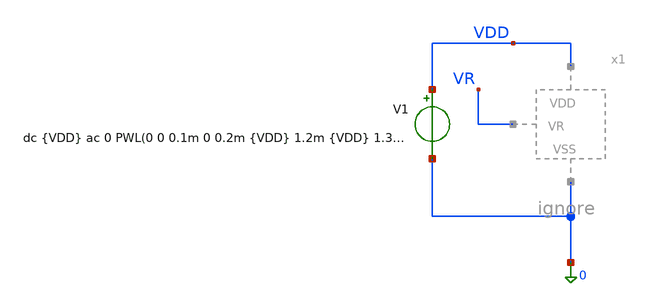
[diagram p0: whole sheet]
** sch_path: xschem/Self_Bias/self_bias_tb_pex_mc.sch
**.subckt self_bias_tb_pex_mc
V1 VDD 0 dc {VDD} ac 0 PWL(0 0 0.1m 0 0.2m {VDD} 1.2m {VDD} 1.3m 0 2m 0 3m {VDD} 4m {VDD} 4.1m 0 5m 0
+ 105m {VDD} 110m {VDD} 110.1m 0)
**** begin user architecture code


* ==============================================================================
* ENCABEZADO DEL ARCHIVO:
* Script de simulación Monte Carlo Post-Layout (PEX) para el circuito Self-Bias.
* Evalúa las 3 rampas de arranque (Trise = 100us, 1ms y 100ms) con tiempos de
* espera recortados (110.1ms totales en lugar de 410ms).
* ==============================================================================

* 1. Librería de modelos Sky130 con Mismatch (tt_mm) y netlist PEX
.lib /foss/pdks/sky130A/libs.tech/ngspice/sky130.lib.spice tt_mm
.include /foss/designs/LDO-sky130/xschem/Self_Bias/self_bias_pex.spice
x1 VDD VR 0 self_bias

.option temp=27
.option num_threads=8
.option gmin=1e-12 reltol=1e-3 abstol=1e-12 vntol=1e-6

* 2. Parámetros globales y condiciones iniciales para el PEX
.param VDD = 1.8
.param rsh_var = agauss(0, 0.005, 1)

.nodeset V(VR)=0.6
.nodeset V(x1.vgp_self)=1.0
.nodeset V(x1.vdi)=0.6
.nodeset V(x1.vdinv)=0.0

.control
let mc_runs = 100
let run = 1

set appendwrite
set filetype=ascii

echo === INICIO MONTE CARLO SELF BIAS PEX === > self_bias_mc.txt

while run <= mc_runs

    echo ======================================
    echo CORRIENDO MONTE CARLO PEX ITERACION: $&run
    echo ======================================
    echo --- ITERACION: $&run --- >> self_bias_mc.txt

    * 1. Resetear variables aleatorias y guardar VDD, VR y los 6 dedos de Mp4
    reset
    save v(VDD) v(vr) @m.x1.x2.msky130_fd_pr__pfet_01v8_lvt[id]
+ @m.x1.x7.msky130_fd_pr__pfet_01v8_lvt[id] @m.x1.x11.msky130_fd_pr__pfet_01v8_lvt[id] @m.x1.x14.msky130_fd_pr__pfet_01v8_lvt[id]
+ @m.x1.x16.msky130_fd_pr__pfet_01v8_lvt[id] @m.x1.x19.msky130_fd_pr__pfet_01v8_lvt[id]

    * 2. Análisis Transitorio corto (110.1ms totales para las 3 rampas)
    tran 1m 110.1m

    * Corriente total IBIAS (suma de los 6 dedos de Mp4 en el PEX)
    let ibias_tot = @m.x1.x2.msky130_fd_pr__pfet_01v8_lvt[id] +
+ @m.x1.x7.msky130_fd_pr__pfet_01v8_lvt[id] + @m.x1.x11.msky130_fd_pr__pfet_01v8_lvt[id] + @m.x1.x14.msky130_fd_pr__pfet_01v8_lvt[id] +
+ @m.x1.x16.msky130_fd_pr__pfet_01v8_lvt[id] + @m.x1.x19.msky130_fd_pr__pfet_01v8_lvt[id]

    write self_bias_mc_tran.raw v(VDD) v(vr) ibias_tot

    * 3. Mediciones en las 3 rampas
    * --- PULSO 1 (Trise = 100us: sube de 0.1m a 0.2m, medimos en 1ms) ---
    meas tran vr_100us FIND v(vr) AT=1m
    meas tran id_100us FIND ibias_tot AT=1m

    * --- PULSO 2 (Trise = 1ms: sube de 2m a 3m, medimos en 3.8ms) ---
    meas tran vr_1ms FIND v(vr) AT=3.8m
    meas tran id_1ms FIND ibias_tot AT=3.8m

    * --- PULSO 3 (Trise = 100ms: sube de 5m a 105m, medimos en 108ms) ---
    meas tran vr_100ms FIND v(vr) AT=108m
    meas tran id_100ms FIND ibias_tot AT=108m

    * Convertir corrientes a microamperios (uA)
    let id_uA_100us = id_100us * 1000000
    let id_uA_1ms   = id_1ms * 1000000
    let id_uA_100ms = id_100ms * 1000000

    * 4. Guardar resultados en el archivo de texto
    echo 'Resultados Iteración $&run:' >> self_bias_mc.txt
    echo '  [100us] VR = $&vr_100us V   | IBIAS = $&id_uA_100us uA' >> self_bias_mc.txt
    echo '  [1ms]   VR = $&vr_1ms V     | IBIAS = $&id_uA_1ms uA' >> self_bias_mc.txt
    echo '  [100ms] VR = $&vr_100ms V   | IBIAS = $&id_uA_100ms uA' >> self_bias_mc.txt
    echo '--------------------------------------' >> self_bias_mc.txt

    let run = run + 1

end

echo === FIN MONTE CARLO SELF BIAS PEX === >> self_bias_mc.txt

.endc


**** end user architecture code
**.ends
.end
